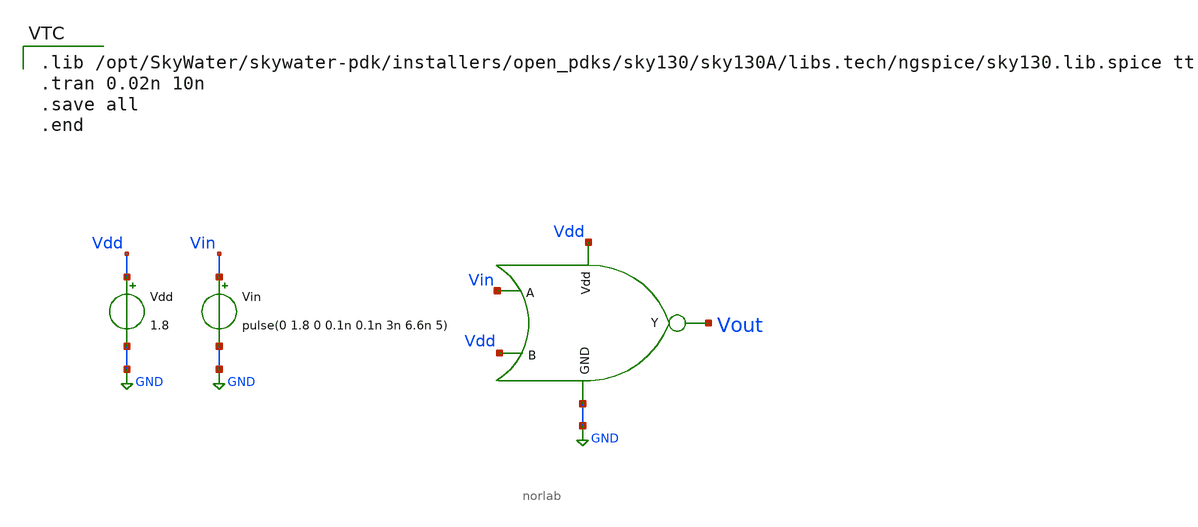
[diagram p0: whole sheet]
** sch_path: 1/xschem/nor_test.sch
**.subckt nor_test
Vdd Vdd GND 1.8
.save i(vdd)
Vin Vin GND pulse(0 1.8 0 0.1n 0.1n 3n 6.6n 5)
.save i(vin)
x2 Vdd Vin net1 Vout GND norlab
**** begin user architecture code

.lib /opt/SkyWater/skywater-pdk/installers/open_pdks/sky130/sky130A/libs.tech/ngspice/sky130.lib.spice tt
.tran 0.02n 10n
.save all
.end

**** end user architecture code
**.ends
.GLOBAL GND
.end
